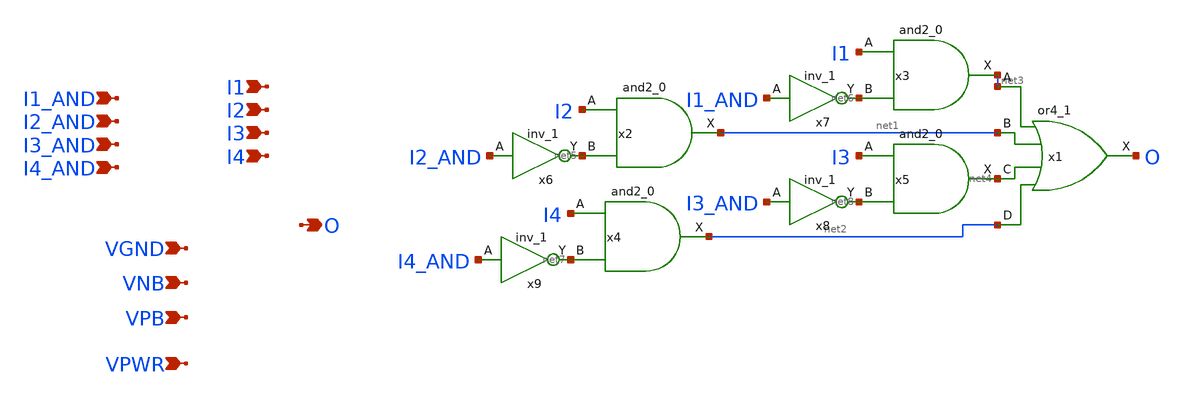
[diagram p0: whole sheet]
** sch_path: schematics/or_4_and_2.sch
**.subckt or_4_and_2 O I1 I2 I3 I4 I1_AND I2_AND I3_AND I4_AND VGND VNB VPB VPWR
*.opin O
*.ipin I1
*.ipin I2
*.ipin I3
*.ipin I4
*.ipin I1_AND
*.ipin I2_AND
*.ipin I3_AND
*.ipin I4_AND
*.ipin VGND
*.ipin VNB
*.ipin VPB
*.ipin VPWR
x1 net3 net1 net4 net2 VGND VNB VPB VPWR O sky130_fd_sc_hd__or4_1
x2 I2 net5 VGND VNB VPB VPWR net1 sky130_fd_sc_hd__and2_0
x3 I1 net6 VGND VNB VPB VPWR net3 sky130_fd_sc_hd__and2_0
x4 I4 net7 VGND VNB VPB VPWR net2 sky130_fd_sc_hd__and2_0
x5 I3 net8 VGND VNB VPB VPWR net4 sky130_fd_sc_hd__and2_0
x6 I2_AND VGND VNB VPB VPWR net5 sky130_fd_sc_hd__inv_1
x7 I1_AND VGND VNB VPB VPWR net6 sky130_fd_sc_hd__inv_1
x8 I3_AND VGND VNB VPB VPWR net8 sky130_fd_sc_hd__inv_1
x9 I4_AND VGND VNB VPB VPWR net7 sky130_fd_sc_hd__inv_1
**.ends
.end
